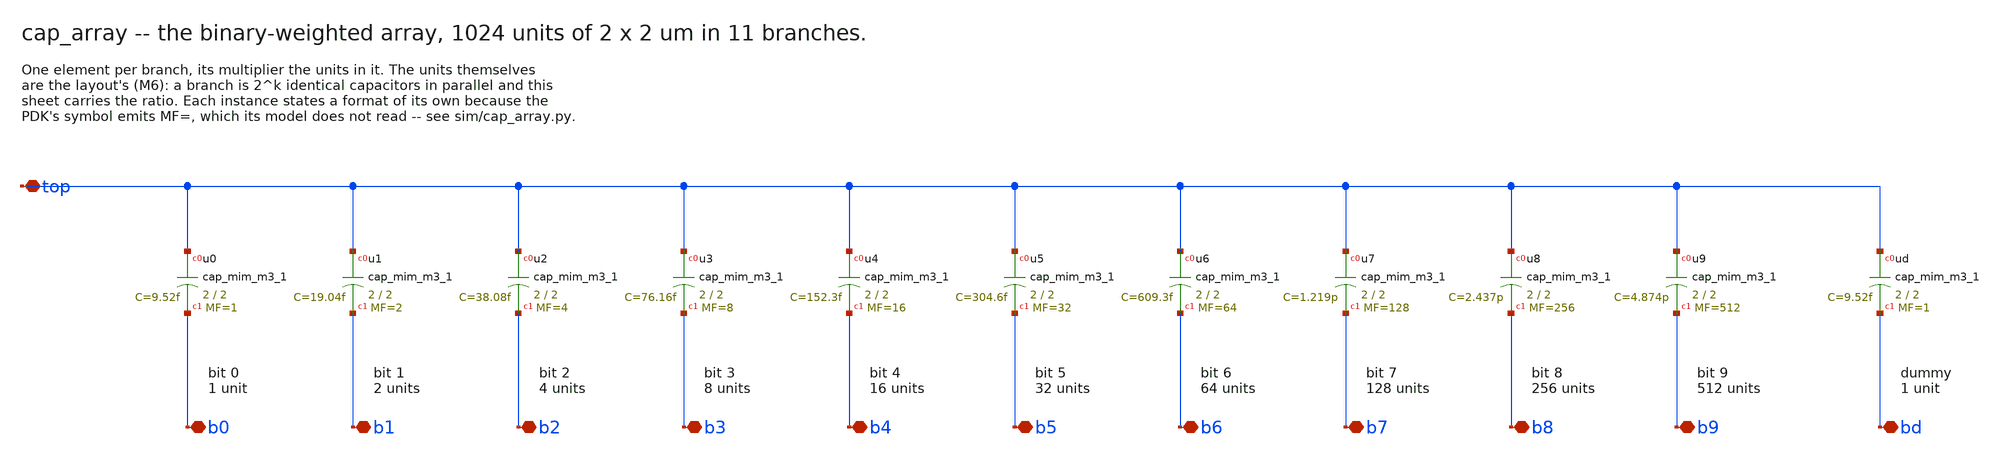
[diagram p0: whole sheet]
** sch_path: xschem/cap_array.sch
**.subckt cap_array top b0 b1 b2 b3 b4 b5 b6 b7 b8 b9 bd
*.iopin top
*.iopin b0
*.iopin b1
*.iopin b2
*.iopin b3
*.iopin b4
*.iopin b5
*.iopin b6
*.iopin b7
*.iopin b8
*.iopin b9
*.iopin bd
Xu0 top b0 sky130_fd_pr__cap_mim_m3_1 w=2 l=2 mult=1 m=1
Xu1 top b1 sky130_fd_pr__cap_mim_m3_1 w=2 l=2 mult=2 m=2
Xu2 top b2 sky130_fd_pr__cap_mim_m3_1 w=2 l=2 mult=4 m=4
Xu3 top b3 sky130_fd_pr__cap_mim_m3_1 w=2 l=2 mult=8 m=8
Xu4 top b4 sky130_fd_pr__cap_mim_m3_1 w=2 l=2 mult=16 m=16
Xu5 top b5 sky130_fd_pr__cap_mim_m3_1 w=2 l=2 mult=32 m=32
Xu6 top b6 sky130_fd_pr__cap_mim_m3_1 w=2 l=2 mult=64 m=64
Xu7 top b7 sky130_fd_pr__cap_mim_m3_1 w=2 l=2 mult=128 m=128
Xu8 top b8 sky130_fd_pr__cap_mim_m3_1 w=2 l=2 mult=256 m=256
Xu9 top b9 sky130_fd_pr__cap_mim_m3_1 w=2 l=2 mult=512 m=512
Xud top bd sky130_fd_pr__cap_mim_m3_1 w=2 l=2 mult=1 m=1
**.ends
.end
